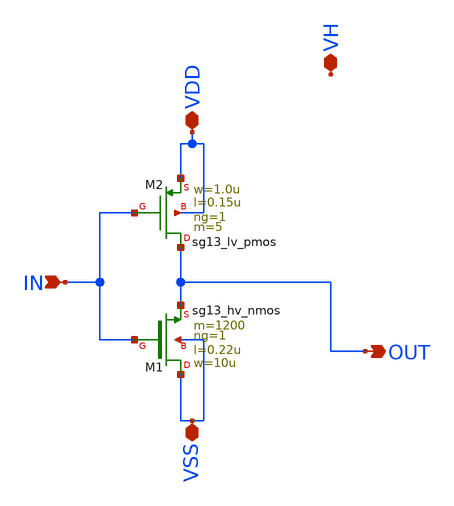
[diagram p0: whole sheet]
** sch_path: xschem/LS_FINAL_IHP.sch
**.subckt LS_FINAL_IHP IN VDD VH OUT VSS
*.ipin IN
*.iopin VDD
*.iopin VH
*.opin OUT
*.iopin VSS
XM2 OUT IN VDD VDD sg13_lv_pmos w=1.0u l=0.15u ng=1 m=5 mm_ok=1
XM1 VSS IN OUT VSS sg13_hv_nmos w=10u l=0.22u ng=1 m=1200 mm_ok=1
**.ends
.end
